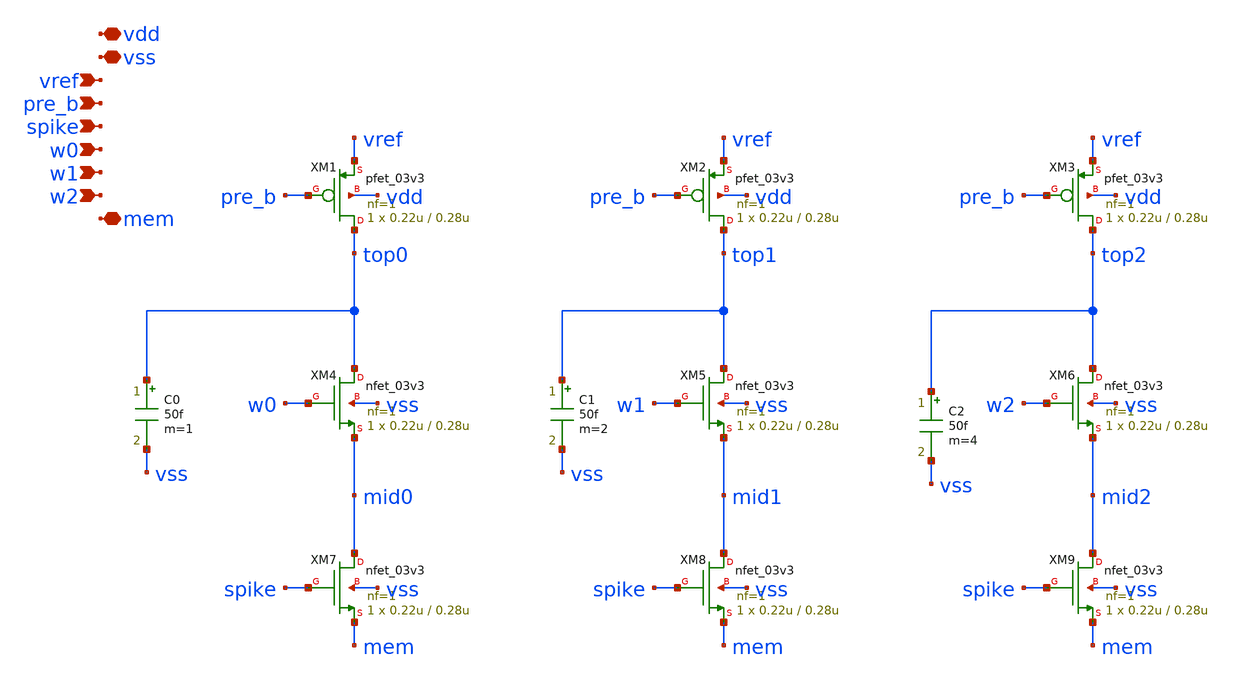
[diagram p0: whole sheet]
** sch_path: analog/dac/charge_injection_DAC.sch
**.subckt charge_injection_DAC vdd vref spike w1 mem vss pre_b w0 w2
*.iopin vdd
*.ipin vref
*.ipin spike
*.ipin w1
*.iopin mem
*.iopin vss
*.ipin pre_b
*.ipin w0
*.ipin w2
XM1 top0 pre_b vref vdd pfet_03v3 L=0.28u W=0.22u nf=1 ad='int((nf+1)/2) * W/nf * 0.18u' as='int((nf+2)/2) * W/nf * 0.18u'
+ pd='2*int((nf+1)/2) * (W/nf + 0.18u)' ps='2*int((nf+2)/2) * (W/nf + 0.18u)' nrd='0.18u / W' nrs='0.18u / W'
+ sa=0 sb=0 sd=0 m=1
C0 top0 vss 50f m=1
XM4 top0 w0 mid0 vss nfet_03v3 L=0.28u W=0.22u nf=1 ad='int((nf+1)/2) * W/nf * 0.18u' as='int((nf+2)/2) * W/nf * 0.18u'
+ pd='2*int((nf+1)/2) * (W/nf + 0.18u)' ps='2*int((nf+2)/2) * (W/nf + 0.18u)' nrd='0.18u / W' nrs='0.18u / W'
+ sa=0 sb=0 sd=0 m=1
XM7 mid0 spike mem vss nfet_03v3 L=0.28u W=0.22u nf=1 ad='int((nf+1)/2) * W/nf * 0.18u' as='int((nf+2)/2) * W/nf * 0.18u'
+ pd='2*int((nf+1)/2) * (W/nf + 0.18u)' ps='2*int((nf+2)/2) * (W/nf + 0.18u)' nrd='0.18u / W' nrs='0.18u / W'
+ sa=0 sb=0 sd=0 m=1
XM2 top1 pre_b vref vdd pfet_03v3 L=0.28u W=0.22u nf=1 ad='int((nf+1)/2) * W/nf * 0.18u' as='int((nf+2)/2) * W/nf * 0.18u'
+ pd='2*int((nf+1)/2) * (W/nf + 0.18u)' ps='2*int((nf+2)/2) * (W/nf + 0.18u)' nrd='0.18u / W' nrs='0.18u / W'
+ sa=0 sb=0 sd=0 m=1
C1 top1 vss 50f m=2
XM5 top1 w1 mid1 vss nfet_03v3 L=0.28u W=0.22u nf=1 ad='int((nf+1)/2) * W/nf * 0.18u' as='int((nf+2)/2) * W/nf * 0.18u'
+ pd='2*int((nf+1)/2) * (W/nf + 0.18u)' ps='2*int((nf+2)/2) * (W/nf + 0.18u)' nrd='0.18u / W' nrs='0.18u / W'
+ sa=0 sb=0 sd=0 m=1
XM8 mid1 spike mem vss nfet_03v3 L=0.28u W=0.22u nf=1 ad='int((nf+1)/2) * W/nf * 0.18u' as='int((nf+2)/2) * W/nf * 0.18u'
+ pd='2*int((nf+1)/2) * (W/nf + 0.18u)' ps='2*int((nf+2)/2) * (W/nf + 0.18u)' nrd='0.18u / W' nrs='0.18u / W'
+ sa=0 sb=0 sd=0 m=1
XM3 top2 pre_b vref vdd pfet_03v3 L=0.28u W=0.22u nf=1 ad='int((nf+1)/2) * W/nf * 0.18u' as='int((nf+2)/2) * W/nf * 0.18u'
+ pd='2*int((nf+1)/2) * (W/nf + 0.18u)' ps='2*int((nf+2)/2) * (W/nf + 0.18u)' nrd='0.18u / W' nrs='0.18u / W'
+ sa=0 sb=0 sd=0 m=1
C2 top2 vss 50f m=4
XM6 top2 w2 mid2 vss nfet_03v3 L=0.28u W=0.22u nf=1 ad='int((nf+1)/2) * W/nf * 0.18u' as='int((nf+2)/2) * W/nf * 0.18u'
+ pd='2*int((nf+1)/2) * (W/nf + 0.18u)' ps='2*int((nf+2)/2) * (W/nf + 0.18u)' nrd='0.18u / W' nrs='0.18u / W'
+ sa=0 sb=0 sd=0 m=1
XM9 mid2 spike mem vss nfet_03v3 L=0.28u W=0.22u nf=1 ad='int((nf+1)/2) * W/nf * 0.18u' as='int((nf+2)/2) * W/nf * 0.18u'
+ pd='2*int((nf+1)/2) * (W/nf + 0.18u)' ps='2*int((nf+2)/2) * (W/nf + 0.18u)' nrd='0.18u / W' nrs='0.18u / W'
+ sa=0 sb=0 sd=0 m=1
**.ends
.end
